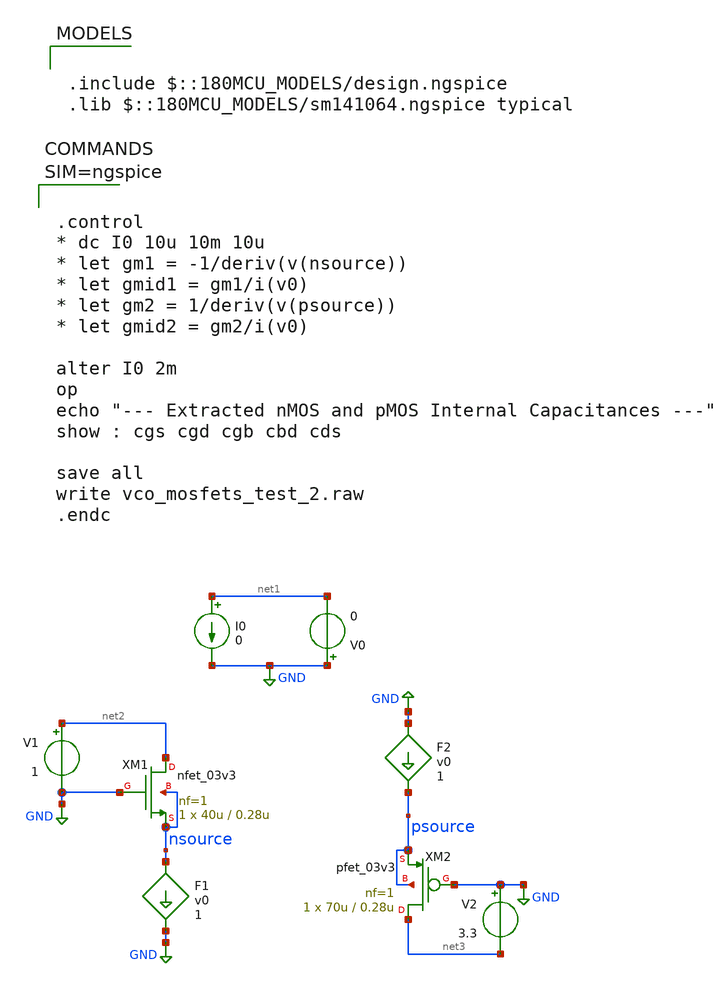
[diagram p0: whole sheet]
** sch_path: team_src/xschem/vco_mosfets_test_2.sch
**.subckt vco_mosfets_test_2
XM1 net2 GND nsource nsource nfet_03v3 L=0.28u W=40u nf=1 ad='int((nf+1)/2) * W/nf * 0.18u' as='int((nf+2)/2) * W/nf * 0.18u'
+ pd='2*int((nf+1)/2) * (W/nf + 0.18u)' ps='2*int((nf+2)/2) * (W/nf + 0.18u)' nrd='0.18u / W' nrs='0.18u / W'
+ sa=0 sb=0 sd=0 m=1
XM2 net3 GND psource psource pfet_03v3 L=0.28u W=70u nf=1 ad='int((nf+1)/2) * W/nf * 0.18u' as='int((nf+2)/2) * W/nf * 0.18u'
+ pd='2*int((nf+1)/2) * (W/nf + 0.18u)' ps='2*int((nf+2)/2) * (W/nf + 0.18u)' nrd='0.18u / W' nrs='0.18u / W'
+ sa=0 sb=0 sd=0 m=1
V0 GND net1 0
F1 nsource GND v0 1
I0 net1 GND 0
V1 net2 GND 1
F2 GND psource v0 1
V2 GND net3 3.3
**** begin user architecture code



.control
* dc I0 10u 10m 10u
* let gm1 = -1/deriv(v(nsource))
* let gmid1 = gm1/i(v0)
* let gm2 = 1/deriv(v(psource))
* let gmid2 = gm2/i(v0)

alter I0 2m
op
echo "--- Extracted nMOS and pMOS Internal Capacitances ---"
show : cgs cgd cgb cbd cds

save all
write vco_mosfets_test_2.raw
.endc




.include $::180MCU_MODELS/design.ngspice
.lib $::180MCU_MODELS/sm141064.ngspice typical

**** end user architecture code
**.ends
.GLOBAL GND
.end
